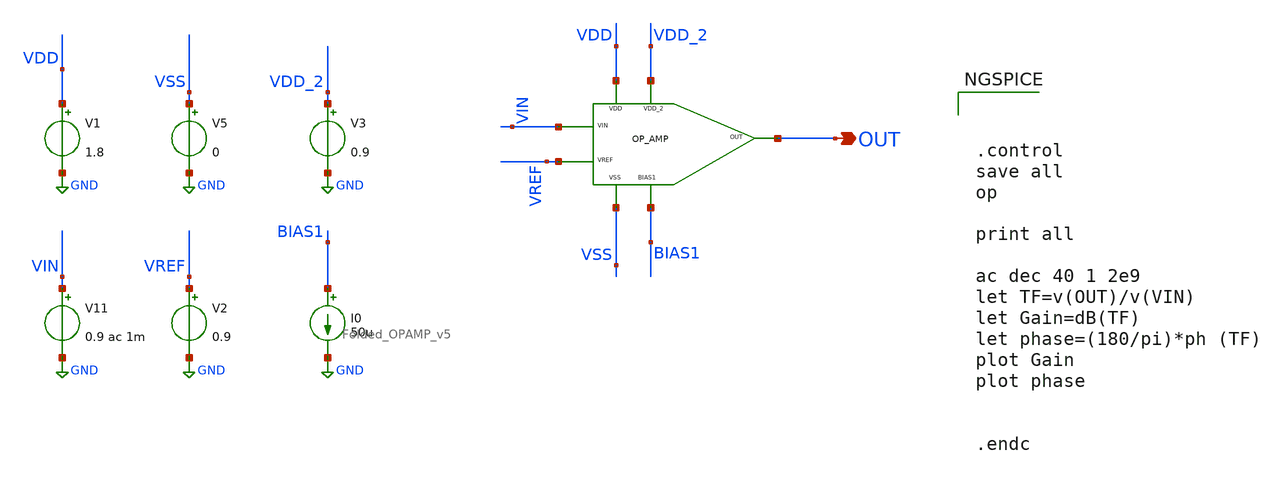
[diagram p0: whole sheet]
** sch_path: xschem/DC_DC_Converter_xschem/OTHERS/DC_DC_Converter_4/Folded_OPAMP/TB_Folded_OPAMP_v5.sch
**.subckt TB_Folded_OPAMP_v5 OUT
*.opin OUT
I0 BIAS1 GND 50u
V1 VDD GND 1.8
V5 VSS GND 0
V11 VIN GND 0.9 ac 1m
V2 VREF GND 0.9
V3 VDD_2 GND 0.9
x1 VDD VSS VDD_2 BIAS1 OUT VIN VREF Folded_OPAMP_v5
**** begin user architecture code

** opencircuitdesign pdks install
.lib $::SKYWATER_MODELS/sky130.lib.spice tt





.control
save all
op

print all

ac dec 40 1 2e9
let TF=v(OUT)/v(VIN)
let Gain=dB(TF)
let phase=(180/pi)*ph (TF)
plot Gain
plot phase


.endc


**** end user architecture code
**.ends

* expanding   symbol:  OTHERS/DC_DC_Converter_4/Folded_OPAMP/Folded_OPAMP_v5.sym # of pins=7
** sym_path: xschem/DC_DC_Converter_xschem/OTHERS/DC_DC_Converter_4/Folded_OPAMP/Folded_OPAMP_v5.sym
** sch_path: xschem/DC_DC_Converter_xschem/OTHERS/DC_DC_Converter_4/Folded_OPAMP/Folded_OPAMP_v5.sch
.subckt Folded_OPAMP_v5 VDD VSS VDD_2 BIAS1 OUT VIN VREF
*.iopin VSS
*.iopin VDD
*.opin OUT
*.ipin VIN
*.ipin VREF
*.iopin BIAS1
*.iopin VDD_2
XM3 VOUTP BIAS1 VDD VDD sky130_fd_pr__pfet_01v8 L=0.9 W=3.91 nf=5 ad='int((nf+1)/2) * W/nf * 0.29' as='int((nf+2)/2) * W/nf * 0.29'
+ pd='2*int((nf+1)/2) * (W/nf + 0.29)' ps='2*int((nf+2)/2) * (W/nf + 0.29)' nrd='0.29 / W' nrs='0.29 / W'
+ sa=0 sb=0 sd=0 mult=5 m=5
XM4 VOUTN BIAS1 VDD VDD sky130_fd_pr__pfet_01v8 L=0.9 W=3.91 nf=5 ad='int((nf+1)/2) * W/nf * 0.29' as='int((nf+2)/2) * W/nf * 0.29'
+ pd='2*int((nf+1)/2) * (W/nf + 0.29)' ps='2*int((nf+2)/2) * (W/nf + 0.29)' nrd='0.29 / W' nrs='0.29 / W'
+ sa=0 sb=0 sd=0 mult=5 m=5
XM6 OUT BIAS2 VOUTN VDD sky130_fd_pr__pfet_01v8 L=0.9 W=3.91 nf=5 ad='int((nf+1)/2) * W/nf * 0.29' as='int((nf+2)/2) * W/nf * 0.29'
+ pd='2*int((nf+1)/2) * (W/nf + 0.29)' ps='2*int((nf+2)/2) * (W/nf + 0.29)' nrd='0.29 / W' nrs='0.29 / W'
+ sa=0 sb=0 sd=0 mult=5 m=5
XM7 net3 BIAS2 VOUTP VDD sky130_fd_pr__pfet_01v8 L=0.9 W=3.91 nf=5 ad='int((nf+1)/2) * W/nf * 0.29' as='int((nf+2)/2) * W/nf * 0.29'
+ pd='2*int((nf+1)/2) * (W/nf + 0.29)' ps='2*int((nf+2)/2) * (W/nf + 0.29)' nrd='0.29 / W' nrs='0.29 / W'
+ sa=0 sb=0 sd=0 mult=5 m=5
XM13 VDD_2 VDD_2 BIAS2 VSS sky130_fd_pr__nfet_01v8 L=0.9 W=5.14 nf=1 ad='int((nf+1)/2) * W/nf * 0.29'
+ as='int((nf+2)/2) * W/nf * 0.29' pd='2*int((nf+1)/2) * (W/nf + 0.29)' ps='2*int((nf+2)/2) * (W/nf + 0.29)'
+ nrd='0.29 / W' nrs='0.29 / W' sa=0 sb=0 sd=0 mult=1 m=1
XM14 BIAS3 BIAS3 net4 VSS sky130_fd_pr__nfet_01v8 L=0.9 W=7.714 nf=10 ad='int((nf+1)/2) * W/nf * 0.29'
+ as='int((nf+2)/2) * W/nf * 0.29' pd='2*int((nf+1)/2) * (W/nf + 0.29)' ps='2*int((nf+2)/2) * (W/nf + 0.29)'
+ nrd='0.29 / W' nrs='0.29 / W' sa=0 sb=0 sd=0 mult=1 m=1
XM15 BIAS2 BIAS2 VSS VSS sky130_fd_pr__nfet_01v8 L=0.9 W=5.14 nf=1 ad='int((nf+1)/2) * W/nf * 0.29' as='int((nf+2)/2) * W/nf * 0.29'
+ pd='2*int((nf+1)/2) * (W/nf + 0.29)' ps='2*int((nf+2)/2) * (W/nf + 0.29)' nrd='0.29 / W' nrs='0.29 / W'
+ sa=0 sb=0 sd=0 mult=1 m=1
XM17 VOUTP VIN net5 VSS sky130_fd_pr__nfet_01v8 L=0.9 W=3.91 nf=1 ad='int((nf+1)/2) * W/nf * 0.29' as='int((nf+2)/2) * W/nf * 0.29'
+ pd='2*int((nf+1)/2) * (W/nf + 0.29)' ps='2*int((nf+2)/2) * (W/nf + 0.29)' nrd='0.29 / W' nrs='0.29 / W'
+ sa=0 sb=0 sd=0 mult=20 m=20
XM18 VOUTN VREF net5 VSS sky130_fd_pr__nfet_01v8 L=0.9 W=3.91 nf=1 ad='int((nf+1)/2) * W/nf * 0.29' as='int((nf+2)/2) * W/nf * 0.29'
+ pd='2*int((nf+1)/2) * (W/nf + 0.29)' ps='2*int((nf+2)/2) * (W/nf + 0.29)' nrd='0.29 / W' nrs='0.29 / W'
+ sa=0 sb=0 sd=0 mult=20 m=20
XM10 OUT BIAS3 net1 VSS sky130_fd_pr__nfet_01v8 L=0.9 W=3.91 nf=5 ad='int((nf+1)/2) * W/nf * 0.29' as='int((nf+2)/2) * W/nf * 0.29'
+ pd='2*int((nf+1)/2) * (W/nf + 0.29)' ps='2*int((nf+2)/2) * (W/nf + 0.29)' nrd='0.29 / W' nrs='0.29 / W'
+ sa=0 sb=0 sd=0 mult=1 m=1
XM12 net3 BIAS3 net2 VSS sky130_fd_pr__nfet_01v8 L=0.9 W=3.91 nf=5 ad='int((nf+1)/2) * W/nf * 0.29' as='int((nf+2)/2) * W/nf * 0.29'
+ pd='2*int((nf+1)/2) * (W/nf + 0.29)' ps='2*int((nf+2)/2) * (W/nf + 0.29)' nrd='0.29 / W' nrs='0.29 / W'
+ sa=0 sb=0 sd=0 mult=1 m=1
XM8 net4 net4 VSS VSS sky130_fd_pr__nfet_01v8 L=0.9 W=7.714 nf=1 ad='int((nf+1)/2) * W/nf * 0.29' as='int((nf+2)/2) * W/nf * 0.29'
+ pd='2*int((nf+1)/2) * (W/nf + 0.29)' ps='2*int((nf+2)/2) * (W/nf + 0.29)' nrd='0.29 / W' nrs='0.29 / W'
+ sa=0 sb=0 sd=0 mult=1 m=1
XM9 net5 net4 VSS VSS sky130_fd_pr__nfet_01v8 L=0.9 W=7.82 nf=1 ad='int((nf+1)/2) * W/nf * 0.29' as='int((nf+2)/2) * W/nf * 0.29'
+ pd='2*int((nf+1)/2) * (W/nf + 0.29)' ps='2*int((nf+2)/2) * (W/nf + 0.29)' nrd='0.29 / W' nrs='0.29 / W'
+ sa=0 sb=0 sd=0 mult=5 m=5
XM5 net2 net3 VSS VSS sky130_fd_pr__nfet_01v8 L=0.9 W=3.91 nf=5 ad='int((nf+1)/2) * W/nf * 0.29' as='int((nf+2)/2) * W/nf * 0.29'
+ pd='2*int((nf+1)/2) * (W/nf + 0.29)' ps='2*int((nf+2)/2) * (W/nf + 0.29)' nrd='0.29 / W' nrs='0.29 / W'
+ sa=0 sb=0 sd=0 mult=1 m=1
XM11 net1 net3 VSS VSS sky130_fd_pr__nfet_01v8 L=0.9 W=3.91 nf=5 ad='int((nf+1)/2) * W/nf * 0.29' as='int((nf+2)/2) * W/nf * 0.29'
+ pd='2*int((nf+1)/2) * (W/nf + 0.29)' ps='2*int((nf+2)/2) * (W/nf + 0.29)' nrd='0.29 / W' nrs='0.29 / W'
+ sa=0 sb=0 sd=0 mult=1 m=1
XM1 BIAS1 BIAS1 VDD VDD sky130_fd_pr__pfet_01v8 L=0.9 W=7.714 nf=1 ad='int((nf+1)/2) * W/nf * 0.29' as='int((nf+2)/2) * W/nf * 0.29'
+ pd='2*int((nf+1)/2) * (W/nf + 0.29)' ps='2*int((nf+2)/2) * (W/nf + 0.29)' nrd='0.29 / W' nrs='0.29 / W'
+ sa=0 sb=0 sd=0 mult=1 m=1
XM2 BIAS3 BIAS1 VDD VDD sky130_fd_pr__pfet_01v8 L=0.9 W=7.714 nf=1 ad='int((nf+1)/2) * W/nf * 0.29' as='int((nf+2)/2) * W/nf * 0.29'
+ pd='2*int((nf+1)/2) * (W/nf + 0.29)' ps='2*int((nf+2)/2) * (W/nf + 0.29)' nrd='0.29 / W' nrs='0.29 / W'
+ sa=0 sb=0 sd=0 mult=1 m=1
.ends

.GLOBAL GND
.end
